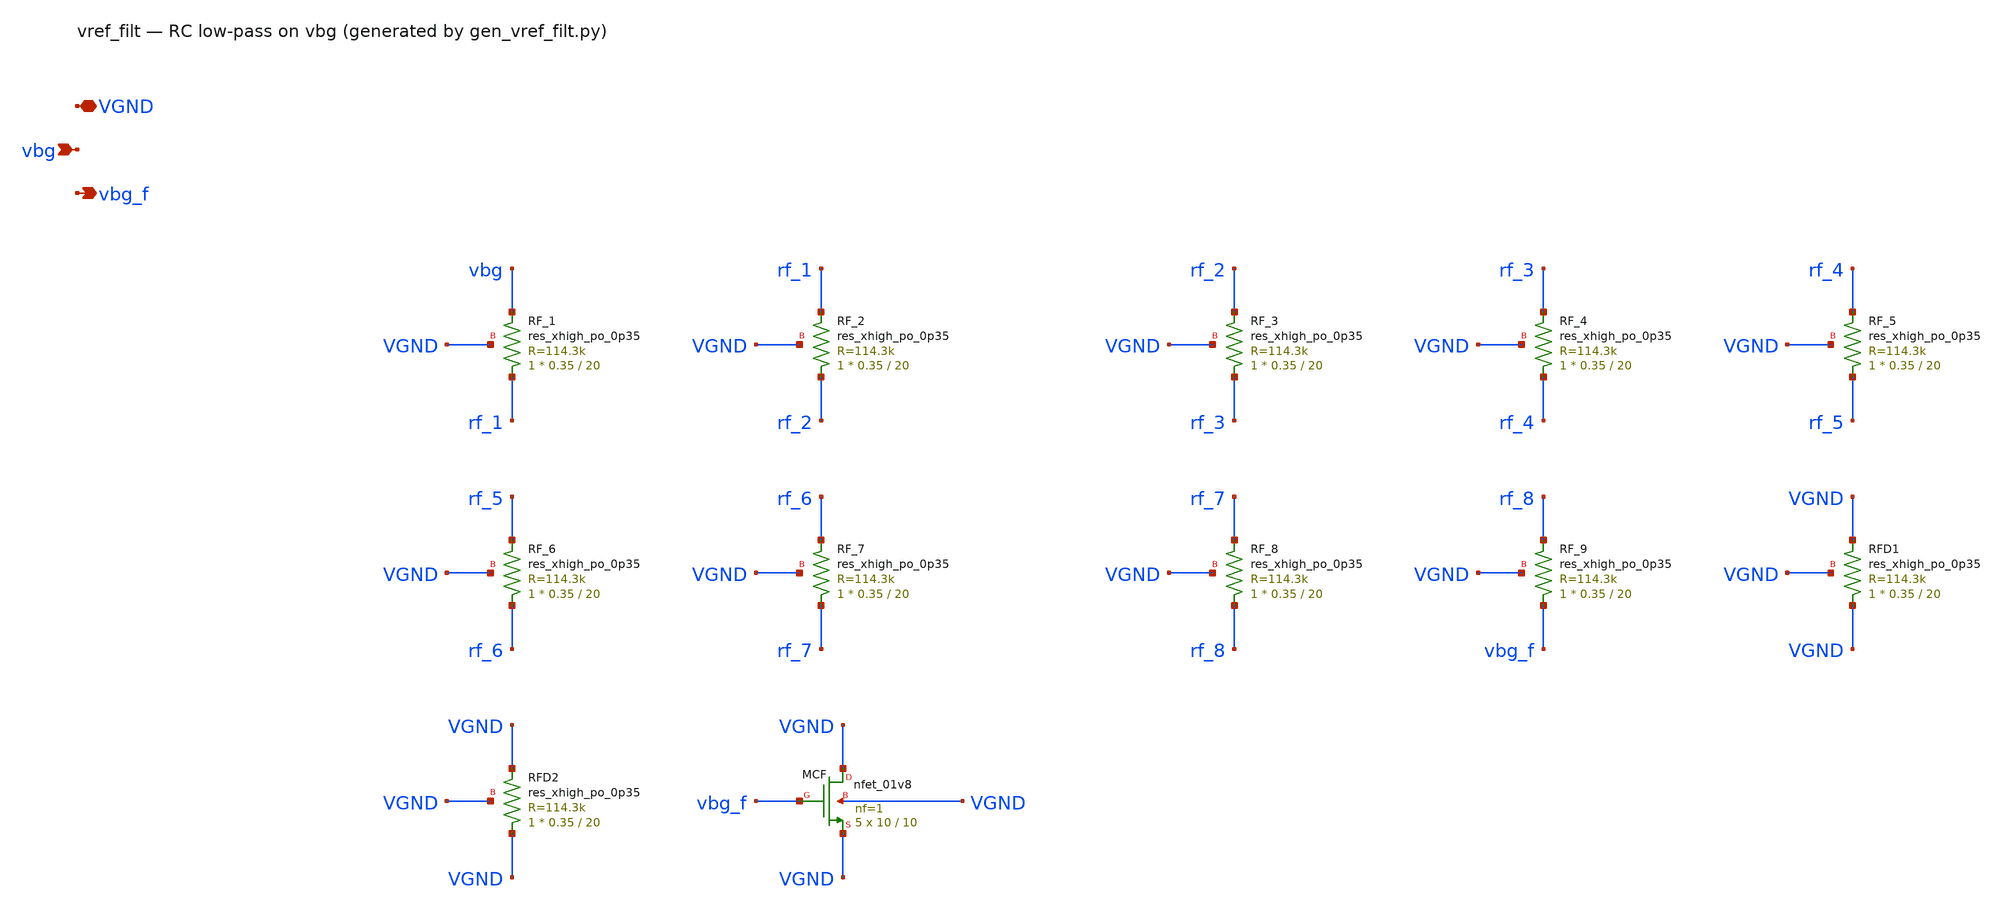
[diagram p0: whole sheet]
** sch_path: xschem/vref_filt.sch
**.subckt vref_filt VGND vbg vbg_f
*.iopin VGND
*.ipin vbg
*.opin vbg_f
XRF_1 rf_1 vbg VGND sky130_fd_pr__res_xhigh_po_0p35 L=20 mult=1 m=1
XRF_2 rf_2 rf_1 VGND sky130_fd_pr__res_xhigh_po_0p35 L=20 mult=1 m=1
XRF_3 rf_3 rf_2 VGND sky130_fd_pr__res_xhigh_po_0p35 L=20 mult=1 m=1
XRF_4 rf_4 rf_3 VGND sky130_fd_pr__res_xhigh_po_0p35 L=20 mult=1 m=1
XRF_5 rf_5 rf_4 VGND sky130_fd_pr__res_xhigh_po_0p35 L=20 mult=1 m=1
XRF_6 rf_6 rf_5 VGND sky130_fd_pr__res_xhigh_po_0p35 L=20 mult=1 m=1
XRF_7 rf_7 rf_6 VGND sky130_fd_pr__res_xhigh_po_0p35 L=20 mult=1 m=1
XRF_8 rf_8 rf_7 VGND sky130_fd_pr__res_xhigh_po_0p35 L=20 mult=1 m=1
XRF_9 vbg_f rf_8 VGND sky130_fd_pr__res_xhigh_po_0p35 L=20 mult=1 m=1
XRFD1 VGND VGND VGND sky130_fd_pr__res_xhigh_po_0p35 L=20 mult=1 m=1
XRFD2 VGND VGND VGND sky130_fd_pr__res_xhigh_po_0p35 L=20 mult=1 m=1
XMCF VGND vbg_f VGND VGND sky130_fd_pr__nfet_01v8 L=10 W=10 nf=1 ad='int((1 + 1)/2) * 10 / 1 * 0.29'
+ as='int((1 + 2)/2) * 10 / 1 * 0.29' pd='2*int((1 + 1)/2) * (10 / 1 + 0.29)' ps='2*int((1 + 2)/2) * (10 / 1 + 0.29)'
+ nrd='0.29 / 10 ' nrs='0.29 / 10 ' sa=0 sb=0 sd=0 mult=5 m=5
**.ends
.end
